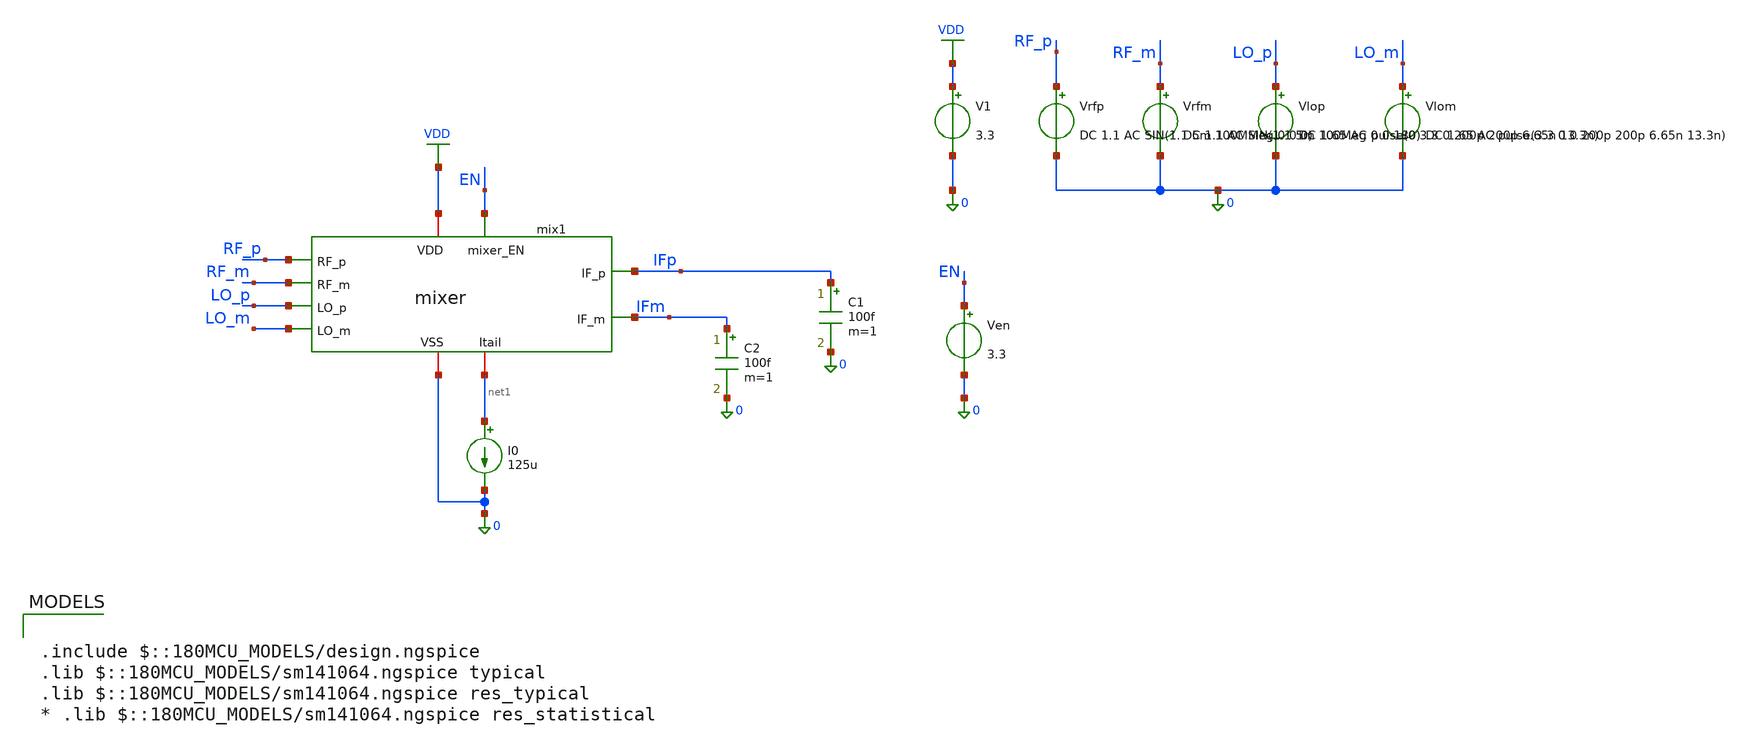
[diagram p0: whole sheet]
** sch_path: designs/mixer/testbench/mixer_with_mirror_tb.sch
**.subckt mixer_with_mirror_tb
V1 VDD 0 3.3
Vrfp RF_p 0 DC 1.1 AC SIN(1.1 5m 100MMeg 0 0 0)
Vrfm RF_m 0 DC 1.1 AC SIN(1.1 5m 100Meg 0 0 180)
Vlop LO_p 0 DC 1.65 AC pulse(0 3.3 0 200p 200p 6.65n 13.3n)
Vlom LO_m 0 DC 1.65 AC pulse(3.3 0 0 200p 200p 6.65n 13.3n)
Ven EN 0 3.3
mix1 IFp RF_p VDD 0 IFm RF_m LO_p net1 LO_m EN mixer
I0 net1 0 125u
C1 IFp 0 100f m=1
C2 IFm 0 100f m=1
**** begin user architecture code

.include $::180MCU_MODELS/design.ngspice
.lib $::180MCU_MODELS/sm141064.ngspice typical
.lib $::180MCU_MODELS/sm141064.ngspice res_typical
* .lib $::180MCU_MODELS/sm141064.ngspice res_statistical




.control

destroy all

write mixer_tb.raw

op
echo RF pair
print @m.x1.xm1.m0[gm]
print @m.x1.xm1.m0[id]
print @m.x1.xm1.m0[vgs]
print @m.x1.xm1.m0[vds]
print @m.x1.xm1.m0[vdsat]

echo LO pair
print @m.x1.xm3.m0[gm]
print @m.x1.xm3.m0[id]
print @m.x1.xm3.m0[vgs]
print @m.x1.xm3.m0[vds]
print @m.x1.xm3.m0[vdsat]

tran 0.01n 2u ;transient sim
let vrf = V(RF_p)-V(RF_m)
let vif = V(IFp)-V(IFm)

plot V(LO_p)
plot vrf
plot vif

fft vif vrf

plot mag(vif) vs frequency
.endc


**** end user architecture code
**.ends

* expanding   symbol:  /foss/designs/NYCMOS/designs/mixer/schematic/mixer.sym # of pins=10
** sym_path: designs/mixer/schematic/mixer.sym
** sch_path: designs/mixer/schematic/mixer.sch
.subckt mixer IF_p RF_p VDD VSS IF_m RF_m LO_p Itail LO_m mixer_EN
*.iopin VDD
*.ipin LO_p
*.ipin LO_m
*.iopin Itail
*.opin IF_m
*.opin IF_p
*.iopin VSS
*.ipin RF_p
*.ipin RF_m
*.ipin mixer_EN
XM1 net1 RF_p net2 VSS nfet_03v3 L=0.28u W=36u nf=6 ad='int((nf+1)/2) * W/nf * 0.18u' as='int((nf+2)/2) * W/nf * 0.18u'
+ pd='2*int((nf+1)/2) * (W/nf + 0.18u)' ps='2*int((nf+2)/2) * (W/nf + 0.18u)' nrd='0.18u / W' nrs='0.18u / W'
+ sa=0 sb=0 sd=0 m=1
XM2 net3 RF_m net2 VSS nfet_03v3 L=0.28u W=36u nf=6 ad='int((nf+1)/2) * W/nf * 0.18u' as='int((nf+2)/2) * W/nf * 0.18u'
+ pd='2*int((nf+1)/2) * (W/nf + 0.18u)' ps='2*int((nf+2)/2) * (W/nf + 0.18u)' nrd='0.18u / W' nrs='0.18u / W'
+ sa=0 sb=0 sd=0 m=1
XM3 IF_m LO_p net1 VSS nfet_03v3 L=0.28u W=21u nf=7 ad='int((nf+1)/2) * W/nf * 0.18u' as='int((nf+2)/2) * W/nf * 0.18u'
+ pd='2*int((nf+1)/2) * (W/nf + 0.18u)' ps='2*int((nf+2)/2) * (W/nf + 0.18u)' nrd='0.18u / W' nrs='0.18u / W'
+ sa=0 sb=0 sd=0 m=1
XM4 IF_p LO_m net1 VSS nfet_03v3 L=0.28u W=21u nf=7 ad='int((nf+1)/2) * W/nf * 0.18u' as='int((nf+2)/2) * W/nf * 0.18u'
+ pd='2*int((nf+1)/2) * (W/nf + 0.18u)' ps='2*int((nf+2)/2) * (W/nf + 0.18u)' nrd='0.18u / W' nrs='0.18u / W'
+ sa=0 sb=0 sd=0 m=1
XM5 IF_m LO_m net3 VSS nfet_03v3 L=0.28u W=21u nf=7 ad='int((nf+1)/2) * W/nf * 0.18u' as='int((nf+2)/2) * W/nf * 0.18u'
+ pd='2*int((nf+1)/2) * (W/nf + 0.18u)' ps='2*int((nf+2)/2) * (W/nf + 0.18u)' nrd='0.18u / W' nrs='0.18u / W'
+ sa=0 sb=0 sd=0 m=1
XM6 IF_p LO_p net3 VSS nfet_03v3 L=0.28u W=21u nf=7 ad='int((nf+1)/2) * W/nf * 0.18u' as='int((nf+2)/2) * W/nf * 0.18u'
+ pd='2*int((nf+1)/2) * (W/nf + 0.18u)' ps='2*int((nf+2)/2) * (W/nf + 0.18u)' nrd='0.18u / W' nrs='0.18u / W'
+ sa=0 sb=0 sd=0 m=1
XM7 net2 mixer_EN Itail VSS nfet_03v3 L=0.28u W=20u nf=4 ad='int((nf+1)/2) * W/nf * 0.18u' as='int((nf+2)/2) * W/nf * 0.18u'
+ pd='2*int((nf+1)/2) * (W/nf + 0.18u)' ps='2*int((nf+2)/2) * (W/nf + 0.18u)' nrd='0.18u / W' nrs='0.18u / W'
+ sa=0 sb=0 sd=0 m=1
XR1 IF_m VDD VSS ppolyf_u_1k r_width=1e-6 r_length=1.8e-6 m=1
XR2 IF_p VDD VSS ppolyf_u_1k r_width=1e-6 r_length=1.8e-6 m=1
.ends

.GLOBAL VDD
.end
